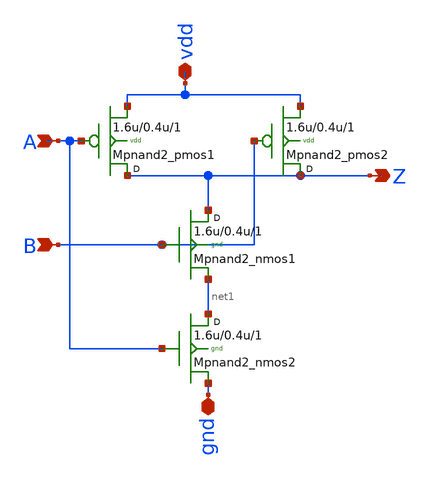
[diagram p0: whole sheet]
** sch_path: sram_2_16_scn4m/pnand2_0.sch
**.subckt pnand2_0 A B Z vdd gnd
*.ipin A
*.ipin B
*.opin Z
*.iopin vdd
*.iopin gnd
Mpnand2_nmos1 Z B net1 gnd n w=1.6u l=0.4u m=1
Mpnand2_pmos1 Z A vdd vdd p w=1.6u l=0.4u m=1
Mpnand2_pmos2 Z B vdd vdd p w=1.6u l=0.4u m=1
Mpnand2_nmos2 net1 A gnd gnd n w=1.6u l=0.4u m=1
**.ends
.end
